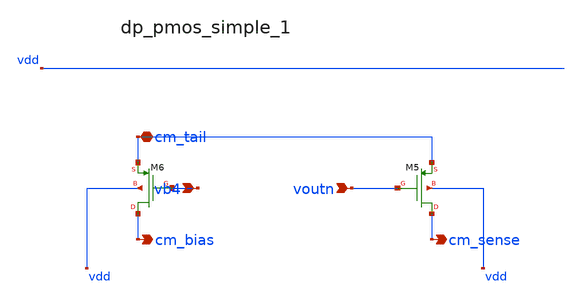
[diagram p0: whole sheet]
** sch_path: analog-db/raw/amp_027_fan_rrl_ota/hier/blocks/dp_pmos_simple_1.sch
**.subckt dp_pmos_simple_1 vb4 voutn cm_tail cm_bias cm_sense
*.ipin vb4
*.ipin voutn
*.iopin cm_tail
*.opin cm_bias
*.opin cm_sense
XM5 cm_sense voutn cm_tail vdd sg13_lv_pmos w=x_dut_xm5_w l=x_dut_xm5_l ng=1 m=x_dut_xm5_m
XM6 cm_bias vb4 cm_tail vdd sg13_lv_pmos w=x_dut_xm6_w l=x_dut_xm6_l ng=1 m=x_dut_xm6_m
**.ends
.end
